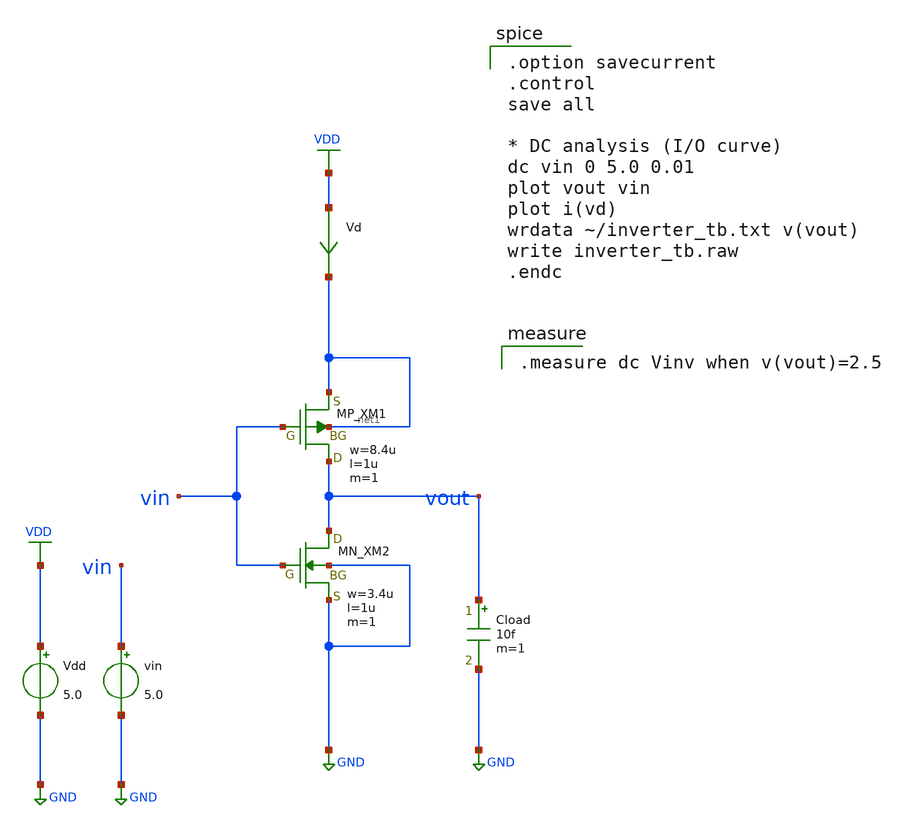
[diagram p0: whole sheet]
** sch_path: inverter/inverter_Takata_Ibuki_tb.sch
**.subckt inverter_Takata_Ibuki_tb
XXM1 vout vin net1 net1 PMOS w=8.4u l=1u nrd=0 nrs=0 m=1
XXM2 vout vin GND GND NMOS w=3.4u l=1u nrd=0 nrs=0 m=1
vin vin GND 5.0
Vd VDD net1 0
.save i(vd)
Cload vout GND 10f m=1
Vdd VDD GND 5.0
**** begin user architecture code
 .include $::LIB/ip62_models

.option savecurrent
.control
save all

* DC analysis (I/O curve)
dc vin 0 5.0 0.01
plot vout vin
plot i(vd)
wrdata ~/inverter_tb.txt v(vout)
write inverter_tb.raw
.endc


.measure dc Vinv when v(vout)=2.5

**** end user architecture code
**.ends
.GLOBAL GND
.GLOBAL VDD
.end
